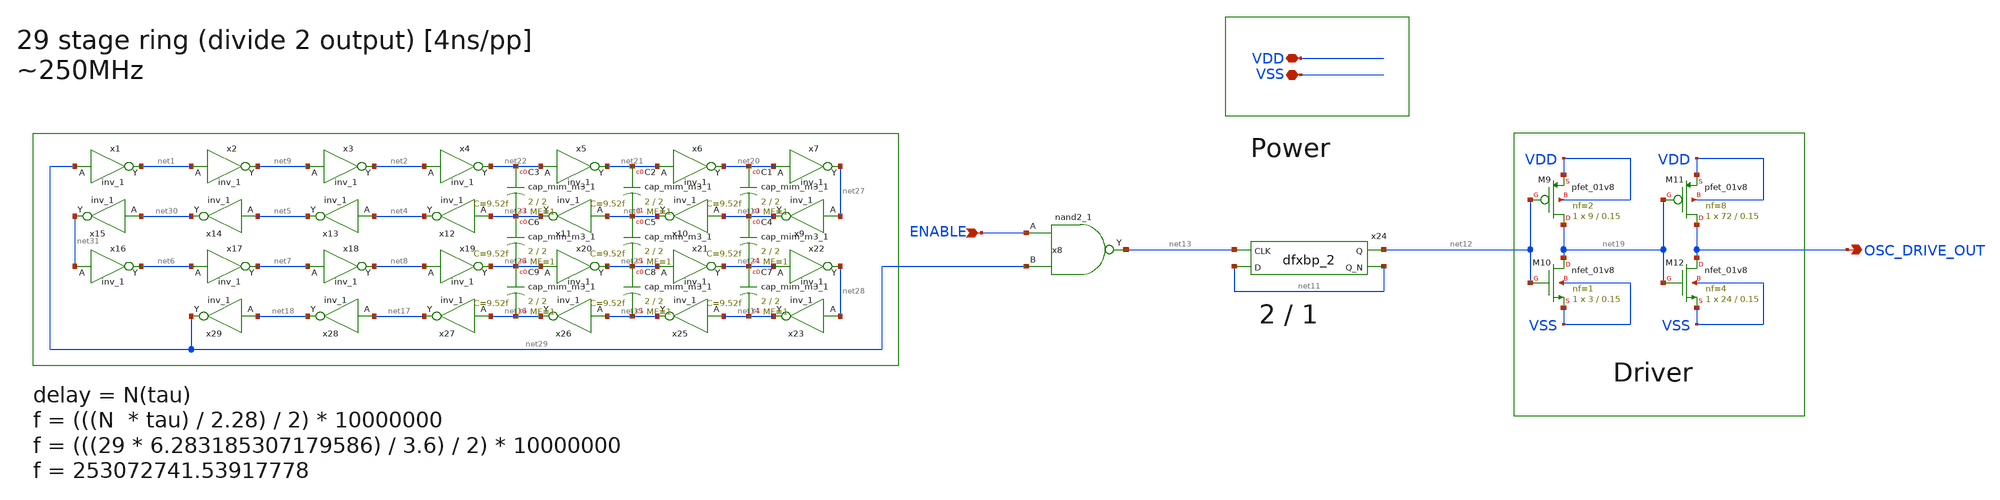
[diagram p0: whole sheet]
** sch_path: xschem/tt-ring-oscillator-test-hd.sch
**.subckt tt-ring-oscillator-test-hd ENABLE VDD VSS OSC_DRIVE_OUT
*.ipin ENABLE
*.iopin VDD
*.iopin VSS
*.opin OSC_DRIVE_OUT
x1 net29 VSS VSS VDD VDD net1 sky130_fd_sc_hd__inv_1
x2 net1 VSS VSS VDD VDD net9 sky130_fd_sc_hd__inv_1
x3 net9 VSS VSS VDD VDD net2 sky130_fd_sc_hd__inv_1
x4 net2 VSS VSS VDD VDD net22 sky130_fd_sc_hd__inv_1
x5 net22 VSS VSS VDD VDD net21 sky130_fd_sc_hd__inv_1
x6 net21 VSS VSS VDD VDD net20 sky130_fd_sc_hd__inv_1
x7 net20 VSS VSS VDD VDD net27 sky130_fd_sc_hd__inv_1
x9 net27 VSS VSS VDD VDD net10 sky130_fd_sc_hd__inv_1
x10 net10 VSS VSS VDD VDD net3 sky130_fd_sc_hd__inv_1
x11 net3 VSS VSS VDD VDD net23 sky130_fd_sc_hd__inv_1
x12 net23 VSS VSS VDD VDD net4 sky130_fd_sc_hd__inv_1
x13 net4 VSS VSS VDD VDD net5 sky130_fd_sc_hd__inv_1
x14 net5 VSS VSS VDD VDD net30 sky130_fd_sc_hd__inv_1
x15 net30 VSS VSS VDD VDD net31 sky130_fd_sc_hd__inv_1
x16 net31 VSS VSS VDD VDD net6 sky130_fd_sc_hd__inv_1
x17 net6 VSS VSS VDD VDD net7 sky130_fd_sc_hd__inv_1
x18 net7 VSS VSS VDD VDD net8 sky130_fd_sc_hd__inv_1
x19 net8 VSS VSS VDD VDD net26 sky130_fd_sc_hd__inv_1
x20 net26 VSS VSS VDD VDD net25 sky130_fd_sc_hd__inv_1
x21 net25 VSS VSS VDD VDD net24 sky130_fd_sc_hd__inv_1
x22 net24 VSS VSS VDD VDD net28 sky130_fd_sc_hd__inv_1
x8 ENABLE net29 VSS VSS VDD VDD net13 sky130_fd_sc_hd__nand2_1
x24 net13 net11 VSS VSS VDD VDD net12 net11 sky130_fd_sc_hd__dfxbp_2
x23 net28 VSS VSS VDD VDD net14 sky130_fd_sc_hd__inv_1
x25 net14 VSS VSS VDD VDD net15 sky130_fd_sc_hd__inv_1
x26 net15 VSS VSS VDD VDD net16 sky130_fd_sc_hd__inv_1
x27 net16 VSS VSS VDD VDD net17 sky130_fd_sc_hd__inv_1
x28 net17 VSS VSS VDD VDD net18 sky130_fd_sc_hd__inv_1
x29 net18 VSS VSS VDD VDD net29 sky130_fd_sc_hd__inv_1
XM9 net19 net12 VDD VDD sky130_fd_pr__pfet_01v8 L=0.15 W=9 nf=2 ad='int((nf+1)/2) * W/nf * 0.29' as='int((nf+2)/2) * W/nf * 0.29'
+ pd='2*int((nf+1)/2) * (W/nf + 0.29)' ps='2*int((nf+2)/2) * (W/nf + 0.29)' nrd='0.29 / W' nrs='0.29 / W'
+ sa=0 sb=0 sd=0 mult=1 m=1
XM10 net19 net12 VSS VSS sky130_fd_pr__nfet_01v8 L=0.15 W=3 nf=1 ad='int((nf+1)/2) * W/nf * 0.29' as='int((nf+2)/2) * W/nf * 0.29'
+ pd='2*int((nf+1)/2) * (W/nf + 0.29)' ps='2*int((nf+2)/2) * (W/nf + 0.29)' nrd='0.29 / W' nrs='0.29 / W'
+ sa=0 sb=0 sd=0 mult=1 m=1
XM11 OSC_DRIVE_OUT net19 VDD VDD sky130_fd_pr__pfet_01v8 L=0.15 W=72 nf=8 ad='int((nf+1)/2) * W/nf * 0.29'
+ as='int((nf+2)/2) * W/nf * 0.29' pd='2*int((nf+1)/2) * (W/nf + 0.29)' ps='2*int((nf+2)/2) * (W/nf + 0.29)'
+ nrd='0.29 / W' nrs='0.29 / W' sa=0 sb=0 sd=0 mult=1 m=1
XM12 OSC_DRIVE_OUT net19 VSS VSS sky130_fd_pr__nfet_01v8 L=0.15 W=24 nf=4 ad='int((nf+1)/2) * W/nf * 0.29'
+ as='int((nf+2)/2) * W/nf * 0.29' pd='2*int((nf+1)/2) * (W/nf + 0.29)' ps='2*int((nf+2)/2) * (W/nf + 0.29)'
+ nrd='0.29 / W' nrs='0.29 / W' sa=0 sb=0 sd=0 mult=1 m=1
XC1 net20 net10 sky130_fd_pr__cap_mim_m3_1 W=2 L=2 MF=1 m=1
XC2 net21 net3 sky130_fd_pr__cap_mim_m3_1 W=2 L=2 MF=1 m=1
XC4 net10 net24 sky130_fd_pr__cap_mim_m3_1 W=2 L=2 MF=1 m=1
XC5 net3 net25 sky130_fd_pr__cap_mim_m3_1 W=2 L=2 MF=1 m=1
XC7 net24 net14 sky130_fd_pr__cap_mim_m3_1 W=2 L=2 MF=1 m=1
XC8 net25 net15 sky130_fd_pr__cap_mim_m3_1 W=2 L=2 MF=1 m=1
XC3 net22 net23 sky130_fd_pr__cap_mim_m3_1 W=2 L=2 MF=1 m=1
XC6 net23 net26 sky130_fd_pr__cap_mim_m3_1 W=2 L=2 MF=1 m=1
XC9 net26 net16 sky130_fd_pr__cap_mim_m3_1 W=2 L=2 MF=1 m=1
**.ends
.end
